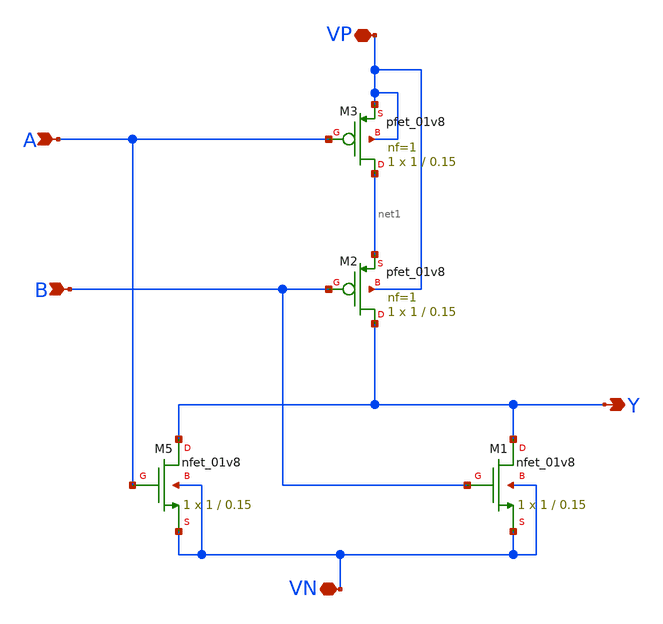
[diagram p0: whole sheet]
** sch_path: nor.sch
**.subckt nor Y VP VN B A
*.opin Y
*.iopin VP
*.iopin VN
*.ipin B
*.ipin A
XM5 Y A VN VN sky130_fd_pr__nfet_01v8 W=1 L=0.15 ad='int((nf+1)/2) * W/nf * 0.29' pd='2*int((nf+1)/2) * (W/nf + 0.29)'
+ as='int((nf+2)/2) * W/nf * 0.29' ps='2*int((nf+2)/2) * (W/nf + 0.29)' nrd='0.29 / W' nrs='0.29 / W' sa=0
+ sb=0 sd=0 nf=1 mult=1
XM1 Y B VN VN sky130_fd_pr__nfet_01v8 W=1 L=0.15 ad='int((nf+1)/2) * W/nf * 0.29' pd='2*int((nf+1)/2) * (W/nf + 0.29)'
+ as='int((nf+2)/2) * W/nf * 0.29' ps='2*int((nf+2)/2) * (W/nf + 0.29)' nrd='0.29 / W' nrs='0.29 / W' sa=0
+ sb=0 sd=0 nf=1 mult=1
XM2 Y B net1 VP sky130_fd_pr__pfet_01v8 L=0.15 W=1 nf=1 ad='int((nf+1)/2) * W/nf * 0.29' as='int((nf+2)/2) * W/nf * 0.29'
+ pd='2*int((nf+1)/2) * (W/nf + 0.29)' ps='2*int((nf+2)/2) * (W/nf + 0.29)' nrd='0.29 / W' nrs='0.29 / W'
+ sa=0 sb=0 sd=0 mult=1 m=1
XM3 net1 A VP VP sky130_fd_pr__pfet_01v8 L=0.15 W=1 nf=1 ad='int((nf+1)/2) * W/nf * 0.29' as='int((nf+2)/2) * W/nf * 0.29'
+ pd='2*int((nf+1)/2) * (W/nf + 0.29)' ps='2*int((nf+2)/2) * (W/nf + 0.29)' nrd='0.29 / W' nrs='0.29 / W'
+ sa=0 sb=0 sd=0 mult=1 m=1
**.ends
.end
